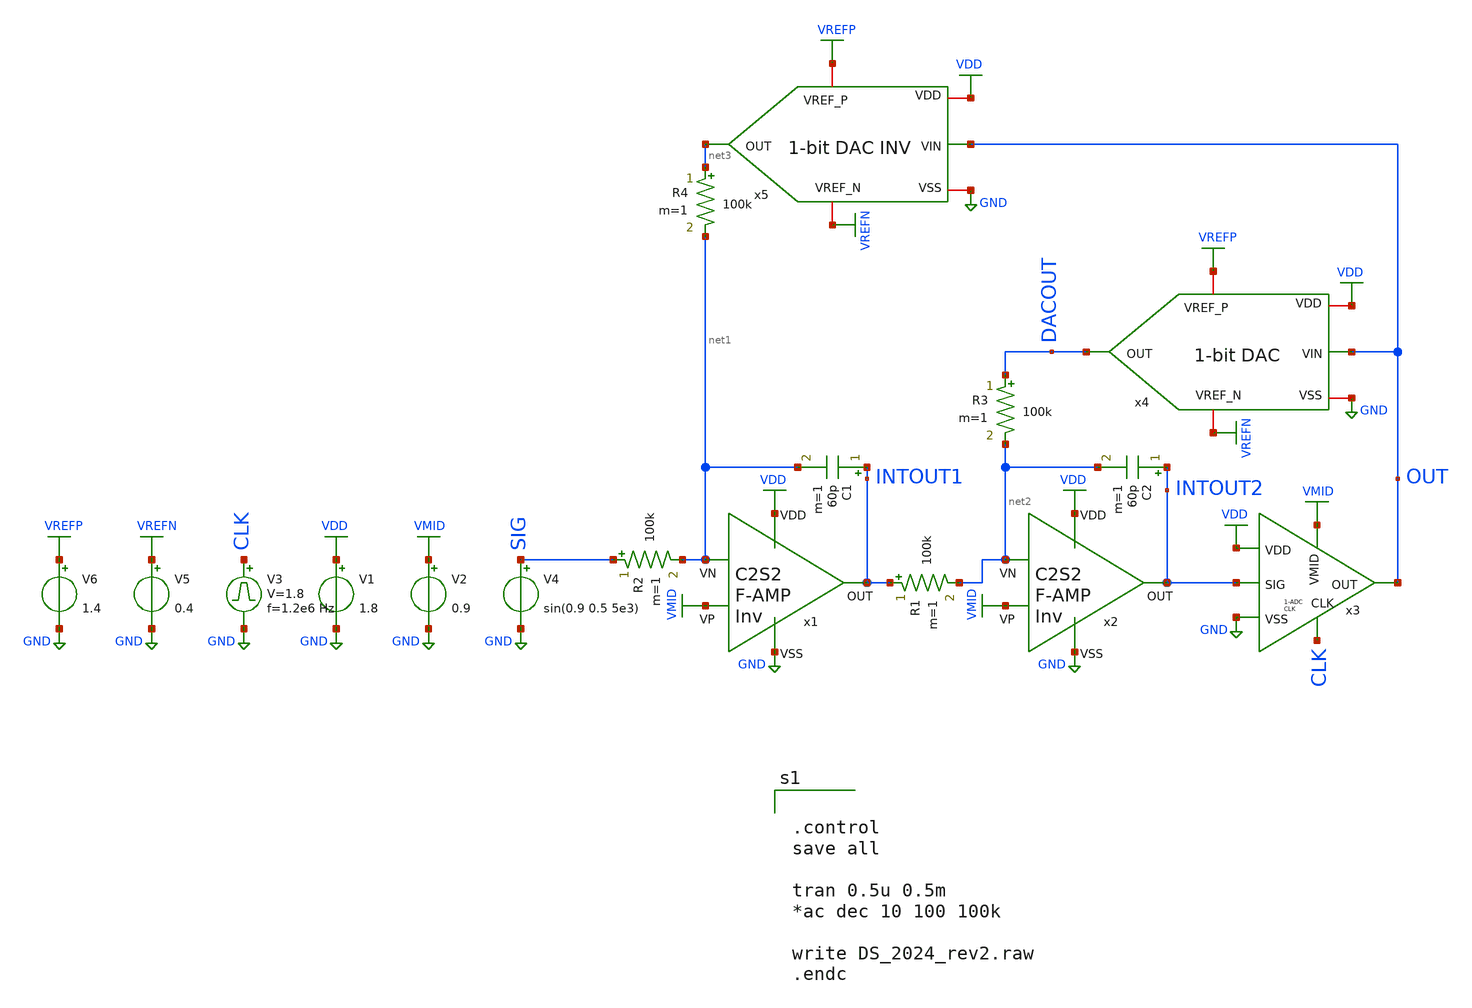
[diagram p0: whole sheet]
** sch_path: SP24_caravel_user_project_analog/xschem/xschem_DeltaSigma/DS_2024_2p0.sch
.lib $::SKYWATER_MODELS/sky130.lib.spice tt
.include $::SKYWATER_STDCELLS/sky130_fd_sc_hd.spice

**.subckt DS_2024_2p0
R1 INTOUT1 net2 100k m=1
R2 SIG net1 100k m=1
R3 DACOUT net2 100k m=1
R4 net3 net1 100k m=1
V1 VDD GND 1.8
V2 VMID GND 0.9
V3 CLK GND pulse 0 1.8 '0.495/ 1.2e6 ' '0.01/1.2e6 ' '0.01/1.2e6 ' '0.49/1.2e6 ' '1/1.2e6 '
V4 SIG GND sin(0.9 0.5 5e3)
C1 INTOUT1 net1 60p m=1
C2 INTOUT2 net2 60p m=1
V5 VREFN GND 0.4
V6 VREFP GND 1.4
x1 VDD VMID net1 INTOUT1 GND C2S2_Amp_F_I
x2 VDD VMID net2 INTOUT2 GND C2S2_Amp_F_I
x5 VREFP VDD net3 OUT GND VREFN 1Bit_DAC_Inv
x4 VREFP VDD DACOUT OUT GND VREFN 1Bit_DAC
x3 VDD INTOUT2 OUT CLK GND VMID 1Bit_Clk_ADC
**** begin user architecture code


.control
save all

tran 0.5u 0.5m
*ac dec 10 100 100k

write DS_2024_rev2.raw
.endc


**** end user architecture code
**.ends
.GLOBAL VDD
.GLOBAL GND
.GLOBAL VMID
.GLOBAL VREFN
.GLOBAL VREFP
.end
